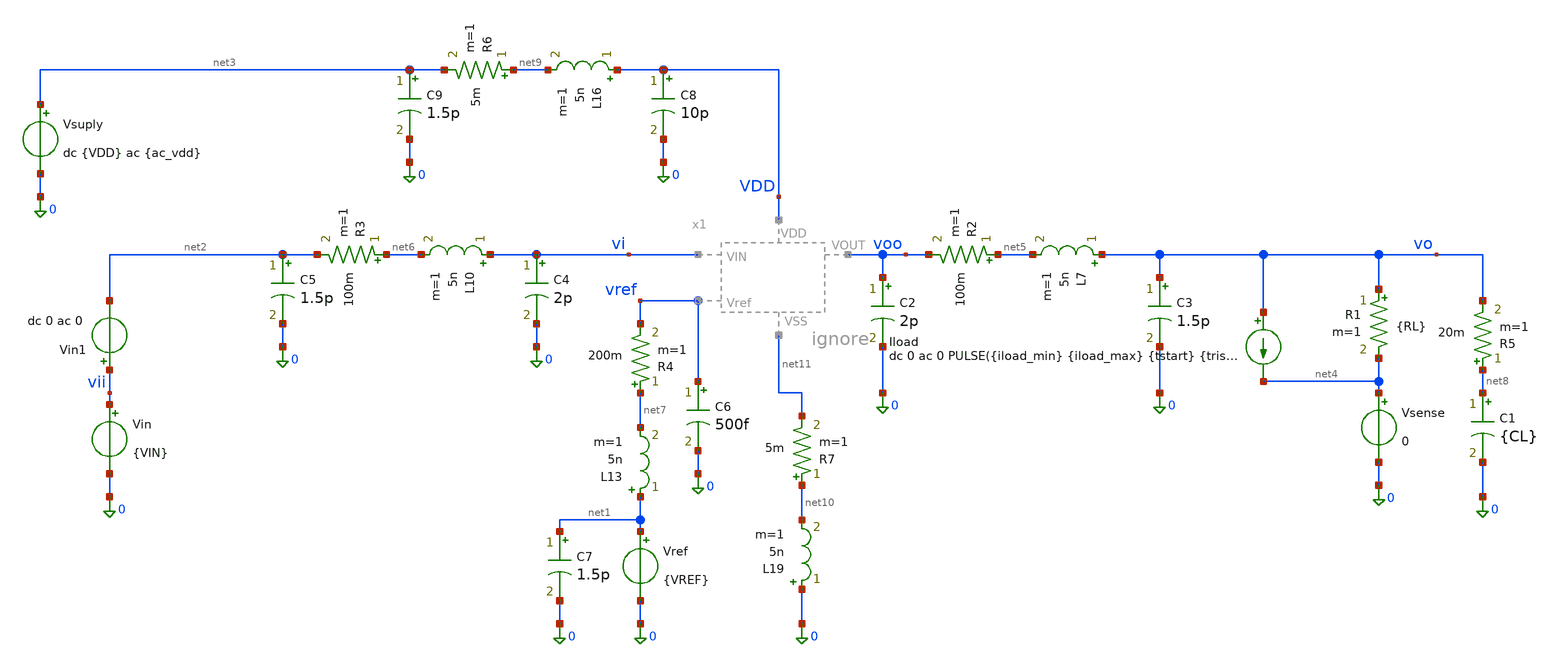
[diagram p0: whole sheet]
** sch_path: xschem/LDO_Top/ldo_tb_pex.sch
**.subckt ldo_tb_pex
Vsuply net3 0 dc {VDD} ac {ac_vdd}
Vref net1 0 {VREF}
Vin vii 0 {VIN}
R1 vo net4 {RL} m=1
C1 net8 0 {CL} m=1
Iload vo net4 dc 0 ac 0 PULSE({iload_min} {iload_max} {tstart} {trise} {tfall} {twidth} {tperiod})
Vsense net4 0 0
Vin1 vii net2 dc 0 ac 0
C2 voo 0 2p m=1
R2 net5 voo 100m m=1
L7 vo net5 5n m=1
C3 vo 0 1.5p m=1
L10 vi net6 5n m=1
C4 vi 0 2p m=1
C5 net2 0 1.5p m=1
R3 net6 net2 100m m=1
L13 net1 net7 5n m=1
R4 net7 vref 200m m=1
C6 vref 0 500f m=1
C7 net1 0 1.5p m=1
R5 net8 vo 20m m=1
L16 VDD net9 5n m=1
C8 VDD 0 10p m=1
C9 net3 0 1.5p m=1
R6 net9 net3 5m m=1
L19 0 net10 5n m=1
R7 net10 net11 5m m=1
**** begin user architecture code


* ==============================================================================
* Encabezado del bloque de simulación: s1 (ldo_tb_pex.sch)
* Descripción:
*   Configuración de simulación post-layout (PEX) para el regulador LDO completo.
*   Incluye la librería Sky130 y el netlist extraído con parásitos (LDO_pex.spice),
*   restringe los vectores guardados en memoria (.save) para evitar desbordamiento
*   de RAM en ngspice, y ejecuta las pruebas de PSRR, Line Regulation,
*   Overshoot/Undershoot, Load Regulation y Dropout (omitiendo AC de estabilidad).
* ==============================================================================

* 1. Inclusión de librería de modelos Sky130 PRIMERO y luego el netlist PEX
.lib /foss/pdks/sky130A/libs.tech/ngspice/sky130.lib.spice tt
.include /foss/designs/LDO-sky130/xschem/LDO_Top/LDO_pex.spice
x1 vi voo VDD vref net11 LDO

.option temp=27
.param VDD = 1.8

.option num_threads=8
.option gmin=1e-12 reltol=1e-3 abstol=1e-12 vntol=1e-6 itl1=500 itl2=200 itl4=100

.param rsh_var = agauss(0, 0.005, 1)

* IMPORTANTE PARA PEX: Guardar únicamente los nodos externos e internos clave
* en lugar de los >35,000 nodos parásitos RC para evitar el error fatal de
* memoria insuficiente en ngspice durante los análisis transitorios.
.save v(vo) v(voo) v(vi) v(vii) v(vdd) v(vref) v(x1.OTA_0.VO_ota) v(x1.OTA_0.VIP_ota) v(x1.self_bias_0.VR) i(Vsuply) i(Vin) i(Vsense)

* Forzar puntos de partida en los nodos reales del PEX para ayudar a la convergencia DC
.nodeset V(vo)=1.2
.nodeset V(voo)=1.2
.nodeset V(x1.OTA_0.VIP_ota)=0.6
.nodeset V(x1.OTA_0.VO_ota)=1.1
.nodeset V(x1.self_bias_0.VR)=0.6
.nodeset V(x1.self_bias_0.vgp_self)=1.0

**parametros_ldo
.param VREF = 0.6
.param VIN = '1*VDD-0.3'
.param RL = 480
.param CL = 1u
.param tsim = 2m

* Parámetros para la prueba de carga del LDO
.param iload_min = 1u
.param iload_max = 5m
.param tstart   = 30u
.param trise    = 100n
.param tfall    = 100n
.param twidth   = 100u
.param tperiod  = 200u

.param tsim = '3*tperiod'

.param ac_iprobe = 0
.param ac_vdd = 0

* --- Clamp SOLO de simulación (evita soluciones DC falsas de cientos de V) ---
* Diodo a tierra: conduce si vo baja de -0.2 V
Dclpn 0 vo dclamp_tb
* Diodo a una fuente de 5 V: conduce si vo sube de 5.7 V
Dclpp vo vclp dclamp_tb
* Clamps en el nodo real de realimentación dentro del PEX (x1.OTA_0.VIP_ota)
Dclpn2 0 x1.OTA_0.VIP_ota dclamp_tb
Dclpp2 x1.OTA_0.VIP_ota vclp dclamp_tb
Vclp vclp 0 5
* Modelo del diodo (fuga ~fA, sin capacitancia: no altera AC ni transitorio)
.model dclamp_tb D(IS=1e-15 N=1)

.control
let tperiod = 200u
let tsim = '3*tperiod'

* =========================================================
* 1. AC (PSRR) -> Genera plot ac1 (se ignora AC de estabilidad)
* =========================================================
alterparam ac_iprobe = 0
alterparam ac_vdd = 1
reset
save v(vo) v(voo) v(vi) v(vii) v(vdd) v(vref) v(x1.OTA_0.VO_ota) v(x1.OTA_0.VIP_ota)
+ v(x1.self_bias_0.VR)

ac dec 10 10 1G

let psrr1 = v(vdd)/v(vo)
let psrr_db = vdb(psrr1)
write LDO_ac_psrr.raw
meas ac gananciaPSRR_1   find psrr_db at=10
meas ac gananciaPSRR_1k  find psrr_db at=1k
meas ac gananciaPSRR_10k find psrr_db at=10k
meas ac gananciaPSRR_1M  find psrr_db at=1Meg

* =========================================================
* 2. TRANSIENTE (Line Regulation) -> Genera plot tran1
* =========================================================
alterparam ac_iprobe = 0
alterparam ac_vdd = 0
reset
save v(vo) v(voo) v(vi) v(vii) v(vdd) v(vref) v(x1.OTA_0.VO_ota) v(x1.OTA_0.VIP_ota)
+ v(x1.self_bias_0.VR)

alter @Vin[pwl] = [ 0 1.4 1m 1.8 ]
alter @Iload[pwl] = [ 0 1u 1m 1u ]

tran 1u 1m
write LDO_dc_line.raw

let t_line_ini = 40u
let t_line_fin = 950u

meas tran voline_max MAX v(vo) from=$&t_line_ini to=$&t_line_fin
meas tran voline_min MIN v(vo) from=$&t_line_ini to=$&t_line_fin
let line_regulation_mV = (voline_max - voline_min)*1000
meas tran salida_line avg v(vo) from=$&t_line_ini to=$&t_line_fin

* =========================================================
* 3. TRANSIENTE (Overshoot y Undershoot) -> Genera plot tran2
* =========================================================
alterparam ac_iprobe = 0
alterparam ac_vdd = 0
alterparam RL = 240e9
reset
save v(vo) v(voo) v(vi) v(vii) v(vdd) v(vref) v(x1.OTA_0.VO_ota) v(x1.OTA_0.VIP_ota)
+ v(x1.self_bias_0.VR)

let tperiod = 200u
let tsim = '3*tperiod'

tran 1u $&tsim
write LDO_tran_picos.raw

let t_ignorar = 150u

meas tran v_estable_ligera FIND v(vo) AT=270u
meas tran v_estable_pesada FIND v(vo) AT=180u
meas tran vo_max MAX v(vo) from=$&t_ignorar to=$&tsim
meas tran vo_min MIN v(vo) from=$&t_ignorar to=$&tsim

let undershoot_mV = (v_estable_ligera - vo_min) * 1e3
let overshoot_mV = (vo_max - v_estable_pesada) * 1e3
meas tran salida_tran avg v(vo) from=$&t_ignorar to=$&tsim

* =========================================================
* 4. TRANSIENTE (Load Regulation) -> Genera plot tran3
* =========================================================
alterparam RL = 240e9
reset
save v(vo) v(voo) v(vi) v(vii) v(vdd) v(vref) v(x1.OTA_0.VO_ota) v(x1.OTA_0.VIP_ota)
+ v(x1.self_bias_0.VR)

alter @Iload[pwl] = [ 0 1u 1m 5m ]

tran 1u 1m
write LDO_dc_load.raw

meas tran vout_light FIND v(vo) AT=40u
meas tran vout_heavy FIND v(vo) AT=1m
let load_regulation_mV = (vout_light - vout_heavy) * 1000

* =========================================================
* 5. TRANSIENTE (Dropout) -> Genera plot tran4
* =========================================================
alterparam RL = 240
reset
save v(vo) v(voo) v(vi) v(vii) v(vdd) v(vref) v(x1.OTA_0.VO_ota) v(x1.OTA_0.VIP_ota)
+ v(x1.self_bias_0.VR)

alter @Vin[pwl] = [ 0 2 1m 0 ]
alter @Iload[pwl] = [ 0 1u 1m 1u ]

tran 1u 1m
write LDO_dc_dropout.raw

meas tran vout_nom FIND v(vo) AT=225u
let vout_target = vout_nom * 0.90
meas tran vin_do FIND v(vi) WHEN v(vo) = vout_target fall=1
let dropout_mV = (vin_do - vout_target) * 1e3

* =========================================================
* IMPRESION DE TODOS LOS RESULTADOS CON SETPLOT
* =========================================================

echo '--- RESULTADOS DE TRANSIENTE (PICOS) ---'
setplot tran2
print undershoot_mV overshoot_mV v_estable_ligera v_estable_pesada salida_tran

echo '--- RESULTADOS AC (PSRR) ---'
setplot ac1
print gananciaPSRR_1 gananciaPSRR_1k gananciaPSRR_10k gananciaPSRR_1M

echo '--- RESULTADOS REGULACIONES Y DROPOUT ---'
echo '>> Line Regulation'
setplot tran1
print line_regulation_mV salida_line

echo '>> Load Regulation'
setplot tran3
print load_regulation_mV

echo '>> Dropout'
setplot tran4
print dropout_mV vin_do vout_target

.endc




* ==============================================================================
* Encabezado del bloque de simulación: s2 (Punto de Operación DC para PEX)
* Descripción:
*   Calcula el punto de operación (.OP) del LDO extraído (LDO_pex.spice) y guarda
*   los voltajes de los nodos principales y los parámetros de los transistores
*   representativos usando sus nombres reales en el netlist plano de Magic.
* ==============================================================================

.control

alterparam RL = 1200
alterparam ac_iprobe = 0
alterparam ac_vdd = 0

reset

* Guardar nodos principales del testbench e internos clave del PEX
save v(vo) v(voo) v(vi) v(vii) v(vdd) v(vref) v(x1.OTA_0.VO_ota) v(x1.OTA_0.VIP_ota) v(x1.OTA_0.vgp)
+ v(x1.OTA_0.vtail) v(x1.OTA_0.vo1) v(x1.self_bias_0.VR) v(x1.self_bias_0.vgp_self) i(Vsuply) i(Vin) i(Vsense)

* Transistores representativos en LDO_pex.spice (mapeados a su instancia plana):
* M1 (transistor de paso PMOS LVT, dedo X1)
save @m.x1.x1.msky130_fd_pr__pfet_01v8_lvt[gm]
save @m.x1.x1.msky130_fd_pr__pfet_01v8_lvt[gds]
save @m.x1.x1.msky130_fd_pr__pfet_01v8_lvt[id]
save @m.x1.x1.msky130_fd_pr__pfet_01v8_lvt[vgs]
save @m.x1.x1.msky130_fd_pr__pfet_01v8_lvt[vds]
save @m.x1.x1.msky130_fd_pr__pfet_01v8_lvt[vth]
save @m.x1.x1.msky130_fd_pr__pfet_01v8_lvt[vdsat]

* Mr (espejo PMOS del OTA, dedo X12)
save @m.x1.x12.msky130_fd_pr__pfet_01v8_lvt[gm]
save @m.x1.x12.msky130_fd_pr__pfet_01v8_lvt[gds]
save @m.x1.x12.msky130_fd_pr__pfet_01v8_lvt[id]
save @m.x1.x12.msky130_fd_pr__pfet_01v8_lvt[vgs]
save @m.x1.x12.msky130_fd_pr__pfet_01v8_lvt[vds]
save @m.x1.x12.msky130_fd_pr__pfet_01v8_lvt[vth]
save @m.x1.x12.msky130_fd_pr__pfet_01v8_lvt[vdsat]

* Mnref (espejo NMOS de entrada de polarización del OTA, X78)
save @m.x1.x78.msky130_fd_pr__nfet_01v8[gm]
save @m.x1.x78.msky130_fd_pr__nfet_01v8[gds]
save @m.x1.x78.msky130_fd_pr__nfet_01v8[id]
save @m.x1.x78.msky130_fd_pr__nfet_01v8[vgs]
save @m.x1.x78.msky130_fd_pr__nfet_01v8[vds]
save @m.x1.x78.msky130_fd_pr__nfet_01v8[vth]
save @m.x1.x78.msky130_fd_pr__nfet_01v8[vdsat]

* --- Etapa Diferencial (Núcleo del OTA) ---
* Mrc1 (fuente de cola PMOS LVT, dedo X15)
save @m.x1.x15.msky130_fd_pr__pfet_01v8_lvt[gm]
save @m.x1.x15.msky130_fd_pr__pfet_01v8_lvt[gds]
save @m.x1.x15.msky130_fd_pr__pfet_01v8_lvt[id]
save @m.x1.x15.msky130_fd_pr__pfet_01v8_lvt[vgs]
save @m.x1.x15.msky130_fd_pr__pfet_01v8_lvt[vds]
save @m.x1.x15.msky130_fd_pr__pfet_01v8_lvt[vth]
save @m.x1.x15.msky130_fd_pr__pfet_01v8_lvt[vdsat]

* Mn (par diferencial entrada VIN_ota/Vref, dedo X22)
save @m.x1.x22.msky130_fd_pr__pfet_01v8_lvt[gm]
save @m.x1.x22.msky130_fd_pr__pfet_01v8_lvt[gds]
save @m.x1.x22.msky130_fd_pr__pfet_01v8_lvt[id]
save @m.x1.x22.msky130_fd_pr__pfet_01v8_lvt[vgs]
save @m.x1.x22.msky130_fd_pr__pfet_01v8_lvt[vds]
save @m.x1.x22.msky130_fd_pr__pfet_01v8_lvt[vth]
save @m.x1.x22.msky130_fd_pr__pfet_01v8_lvt[vdsat]

* Mp (par diferencial entrada VIP_ota, dedo X14)
save @m.x1.x14.msky130_fd_pr__pfet_01v8_lvt[gm]
save @m.x1.x14.msky130_fd_pr__pfet_01v8_lvt[gds]
save @m.x1.x14.msky130_fd_pr__pfet_01v8_lvt[id]
save @m.x1.x14.msky130_fd_pr__pfet_01v8_lvt[vgs]
save @m.x1.x14.msky130_fd_pr__pfet_01v8_lvt[vds]
save @m.x1.x14.msky130_fd_pr__pfet_01v8_lvt[vth]
save @m.x1.x14.msky130_fd_pr__pfet_01v8_lvt[vdsat]

* Mnr (carga activa NMOS en diodo, dedo X48)
save @m.x1.x48.msky130_fd_pr__nfet_01v8[gm]
save @m.x1.x48.msky130_fd_pr__nfet_01v8[gds]
save @m.x1.x48.msky130_fd_pr__nfet_01v8[id]
save @m.x1.x48.msky130_fd_pr__nfet_01v8[vgs]
save @m.x1.x48.msky130_fd_pr__nfet_01v8[vds]
save @m.x1.x48.msky130_fd_pr__nfet_01v8[vth]
save @m.x1.x48.msky130_fd_pr__nfet_01v8[vdsat]

* Mpr (carga activa NMOS salida vo1, dedo X92)
save @m.x1.x92.msky130_fd_pr__nfet_01v8[gm]
save @m.x1.x92.msky130_fd_pr__nfet_01v8[gds]
save @m.x1.x92.msky130_fd_pr__nfet_01v8[id]
save @m.x1.x92.msky130_fd_pr__nfet_01v8[vgs]
save @m.x1.x92.msky130_fd_pr__nfet_01v8[vds]
save @m.x1.x92.msky130_fd_pr__nfet_01v8[vth]
save @m.x1.x92.msky130_fd_pr__nfet_01v8[vdsat]

* --- Etapa de Salida del OTA ---
* Mrc2 (carga PMOS etapa de salida, dedo X52)
save @m.x1.x52.msky130_fd_pr__pfet_01v8_lvt[gm]
save @m.x1.x52.msky130_fd_pr__pfet_01v8_lvt[gds]
save @m.x1.x52.msky130_fd_pr__pfet_01v8_lvt[id]
save @m.x1.x52.msky130_fd_pr__pfet_01v8_lvt[vgs]
save @m.x1.x52.msky130_fd_pr__pfet_01v8_lvt[vds]
save @m.x1.x52.msky130_fd_pr__pfet_01v8_lvt[vth]
save @m.x1.x52.msky130_fd_pr__pfet_01v8_lvt[vdsat]

* Mo (transistor NMOS etapa de salida, dedo X6)
save @m.x1.x6.msky130_fd_pr__nfet_01v8[gm]
save @m.x1.x6.msky130_fd_pr__nfet_01v8[gds]
save @m.x1.x6.msky130_fd_pr__nfet_01v8[id]
save @m.x1.x6.msky130_fd_pr__nfet_01v8[vgs]
save @m.x1.x6.msky130_fd_pr__nfet_01v8[vds]
save @m.x1.x6.msky130_fd_pr__nfet_01v8[vth]
save @m.x1.x6.msky130_fd_pr__nfet_01v8[vdsat]

op
set filetype=ascii
write LDO_op.raw

.endc


**** end user architecture code
**.ends
.end
